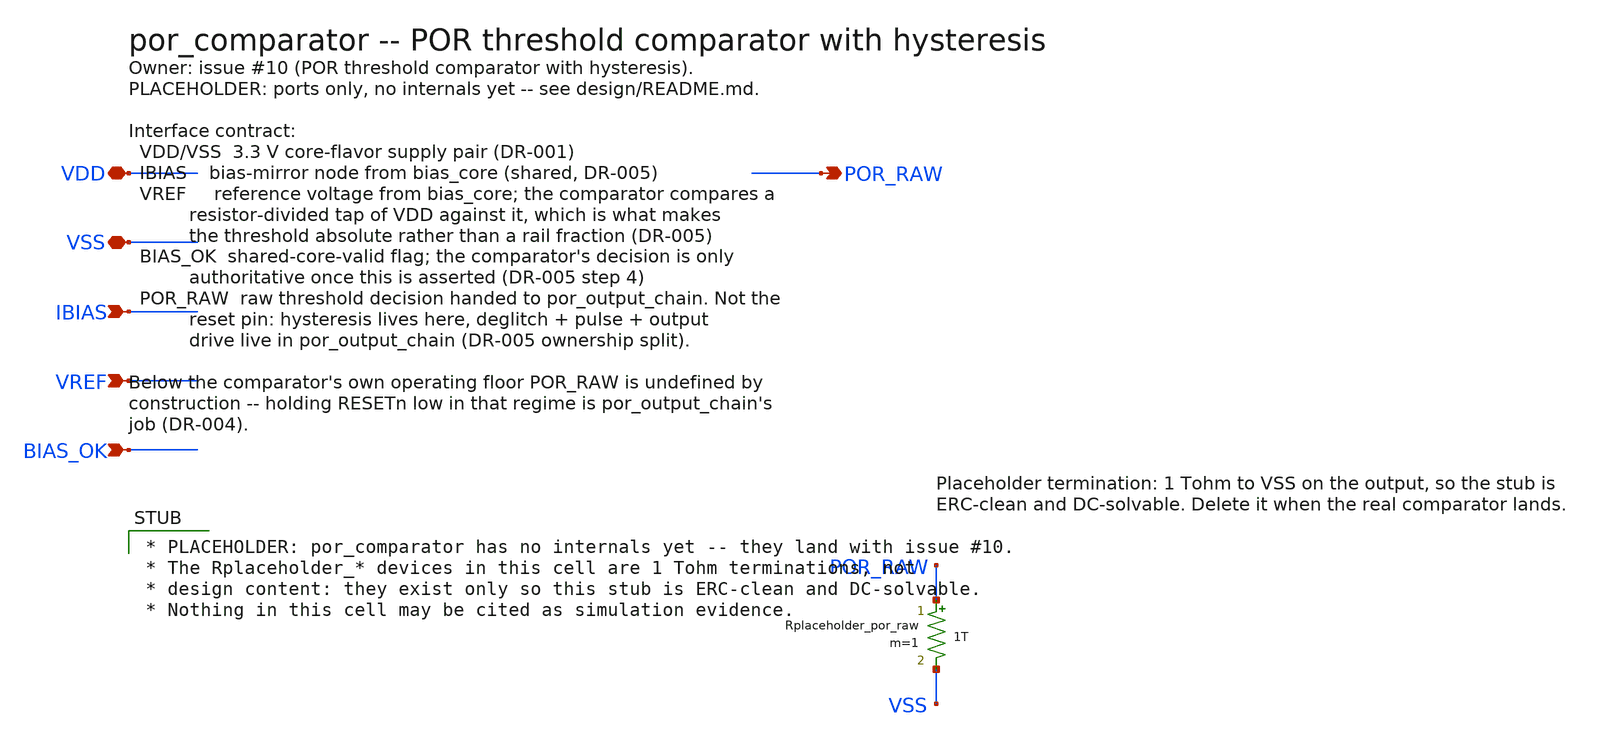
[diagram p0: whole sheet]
** sch_path: design/por_comparator.sch
**.subckt por_comparator VDD VSS IBIAS VREF BIAS_OK POR_RAW
*.iopin VDD
*.iopin VSS
*.ipin IBIAS
*.ipin VREF
*.ipin BIAS_OK
*.opin POR_RAW
Rplaceholder_por_raw POR_RAW VSS 1T m=1
**** begin user architecture code

* PLACEHOLDER: por_comparator has no internals yet -- they land with issue #10.
* The Rplaceholder_* devices in this cell are 1 Tohm terminations, not
* design content: they exist only so this stub is ERC-clean and DC-solvable.
* Nothing in this cell may be cited as simulation evidence.

**** end user architecture code
**.ends
.end
